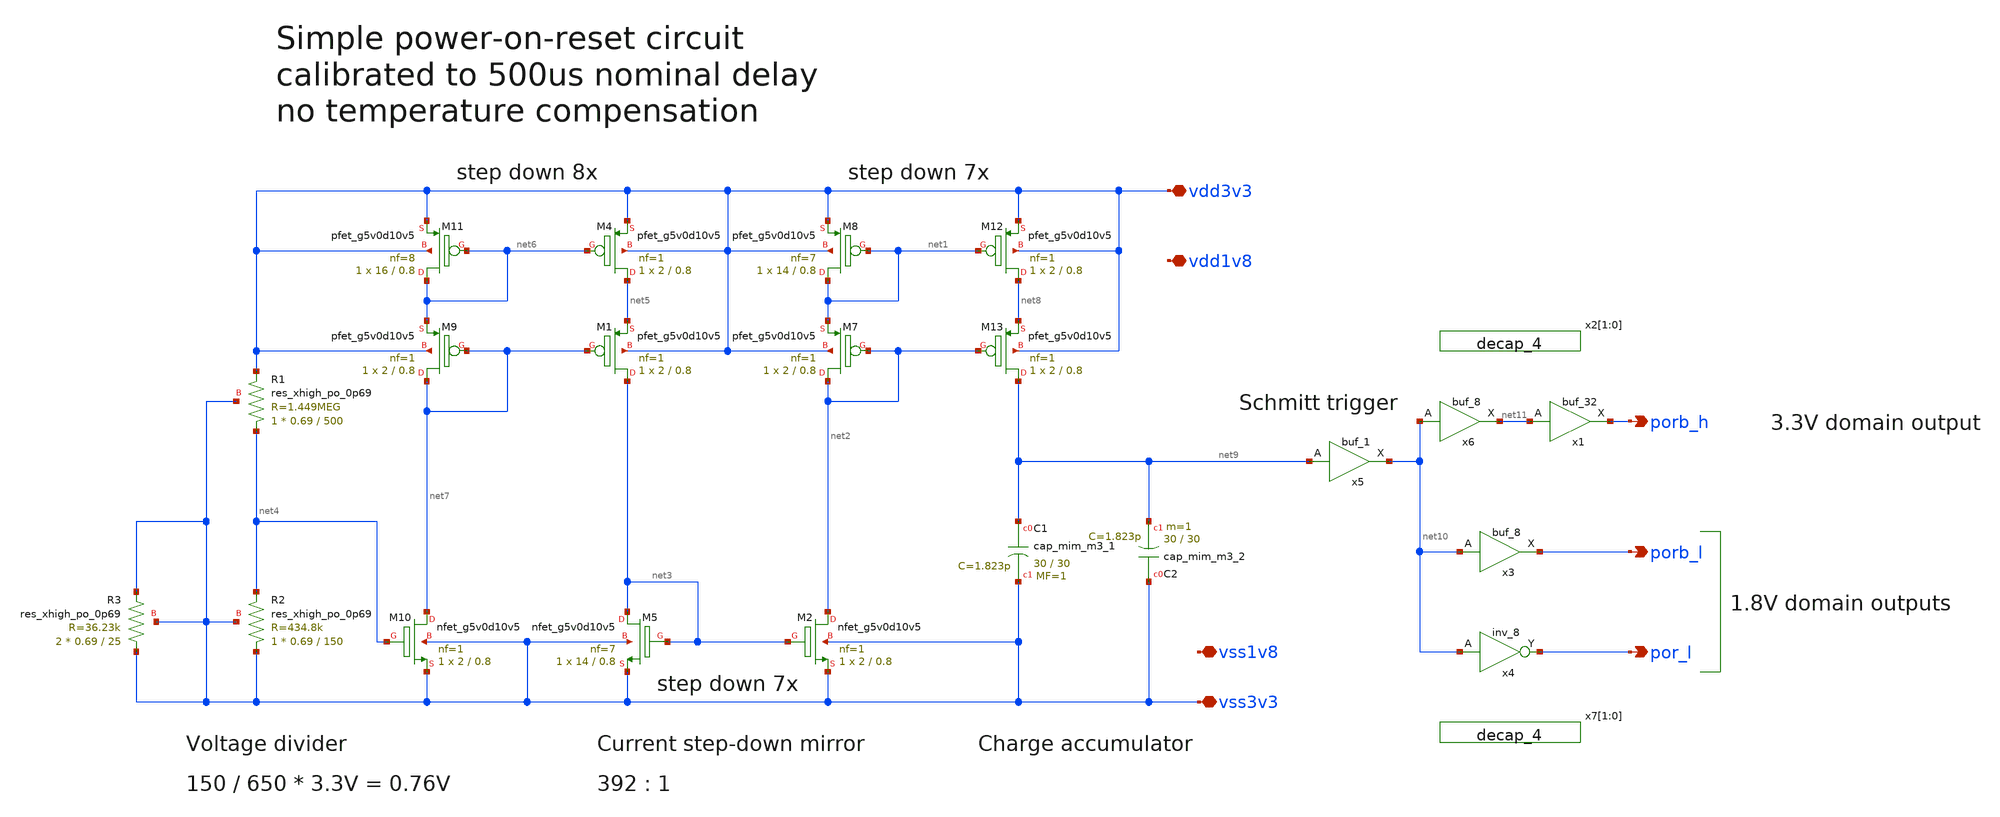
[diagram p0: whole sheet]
** sch_path: xschem/sky130_ef_ip__simple_por4x.sch
**.subckt sky130_ef_ip__simple_por4x vdd3v3 vss3v3 porb_l por_l vdd1v8 vss1v8 porb_h
*.iopin vdd3v3
*.iopin vss3v3
*.opin porb_l
*.opin por_l
*.iopin vdd1v8
*.iopin vss1v8
*.opin porb_h
XC1 net9 vss3v3 sky130_fd_pr__cap_mim_m3_1 W=30 L=30 MF=1 m=1
XC2 vss3v3 net9 sky130_fd_pr__cap_mim_m3_2 W=30 L=30 MF=1 m=1
XM1 net3 net7 net5 vdd3v3 sky130_fd_pr__pfet_g5v0d10v5 L=0.8 W=2 nf=1 ad='int((nf+1)/2) * W/nf * 0.29'
+ as='int((nf+2)/2) * W/nf * 0.29' pd='2*int((nf+1)/2) * (W/nf + 0.29)' ps='2*int((nf+2)/2) * (W/nf + 0.29)'
+ nrd='0.29 / W' nrs='0.29 / W' sa=0 sb=0 sd=0 mult=1 m=1
XM2 net2 net3 vss3v3 vss3v3 sky130_fd_pr__nfet_g5v0d10v5 L=0.8 W=2 nf=1 ad='int((nf+1)/2) * W/nf * 0.29'
+ as='int((nf+2)/2) * W/nf * 0.29' pd='2*int((nf+1)/2) * (W/nf + 0.29)' ps='2*int((nf+2)/2) * (W/nf + 0.29)'
+ nrd='0.29 / W' nrs='0.29 / W' sa=0 sb=0 sd=0 mult=1 m=1
XR1 net4 vdd3v3 vss3v3 sky130_fd_pr__res_xhigh_po_0p69 L=500 mult=1 m=1
XM4 net5 net6 vdd3v3 vdd3v3 sky130_fd_pr__pfet_g5v0d10v5 L=0.8 W=2 nf=1 ad='int((nf+1)/2) * W/nf * 0.29'
+ as='int((nf+2)/2) * W/nf * 0.29' pd='2*int((nf+1)/2) * (W/nf + 0.29)' ps='2*int((nf+2)/2) * (W/nf + 0.29)'
+ nrd='0.29 / W' nrs='0.29 / W' sa=0 sb=0 sd=0 mult=1 m=1
XM5 net3 net3 vss3v3 vss3v3 sky130_fd_pr__nfet_g5v0d10v5 L=0.8 W=14 nf=7 ad='int((nf+1)/2) * W/nf * 0.29'
+ as='int((nf+2)/2) * W/nf * 0.29' pd='2*int((nf+1)/2) * (W/nf + 0.29)' ps='2*int((nf+2)/2) * (W/nf + 0.29)'
+ nrd='0.29 / W' nrs='0.29 / W' sa=0 sb=0 sd=0 mult=1 m=1
XR2 vss3v3 net4 vss3v3 sky130_fd_pr__res_xhigh_po_0p69 L=150 mult=1 m=1
XM7 net2 net2 net1 vdd3v3 sky130_fd_pr__pfet_g5v0d10v5 L=0.8 W=2 nf=1 ad='int((nf+1)/2) * W/nf * 0.29'
+ as='int((nf+2)/2) * W/nf * 0.29' pd='2*int((nf+1)/2) * (W/nf + 0.29)' ps='2*int((nf+2)/2) * (W/nf + 0.29)'
+ nrd='0.29 / W' nrs='0.29 / W' sa=0 sb=0 sd=0 mult=1 m=1
XM8 net1 net1 vdd3v3 vdd3v3 sky130_fd_pr__pfet_g5v0d10v5 L=0.8 W=14 nf=7 ad='int((nf+1)/2) * W/nf * 0.29'
+ as='int((nf+2)/2) * W/nf * 0.29' pd='2*int((nf+1)/2) * (W/nf + 0.29)' ps='2*int((nf+2)/2) * (W/nf + 0.29)'
+ nrd='0.29 / W' nrs='0.29 / W' sa=0 sb=0 sd=0 mult=1 m=1
XM10 net7 net4 vss3v3 vss3v3 sky130_fd_pr__nfet_g5v0d10v5 L=0.8 W=2 nf=1 ad='int((nf+1)/2) * W/nf * 0.29'
+ as='int((nf+2)/2) * W/nf * 0.29' pd='2*int((nf+1)/2) * (W/nf + 0.29)' ps='2*int((nf+2)/2) * (W/nf + 0.29)'
+ nrd='0.29 / W' nrs='0.29 / W' sa=0 sb=0 sd=0 mult=1 m=1
XM9 net7 net7 net6 vdd3v3 sky130_fd_pr__pfet_g5v0d10v5 L=0.8 W=2 nf=1 ad='int((nf+1)/2) * W/nf * 0.29'
+ as='int((nf+2)/2) * W/nf * 0.29' pd='2*int((nf+1)/2) * (W/nf + 0.29)' ps='2*int((nf+2)/2) * (W/nf + 0.29)'
+ nrd='0.29 / W' nrs='0.29 / W' sa=0 sb=0 sd=0 mult=1 m=1
XM11 net6 net6 vdd3v3 vdd3v3 sky130_fd_pr__pfet_g5v0d10v5 L=0.8 W=16 nf=8 ad='int((nf+1)/2) * W/nf * 0.29'
+ as='int((nf+2)/2) * W/nf * 0.29' pd='2*int((nf+1)/2) * (W/nf + 0.29)' ps='2*int((nf+2)/2) * (W/nf + 0.29)'
+ nrd='0.29 / W' nrs='0.29 / W' sa=0 sb=0 sd=0 mult=1 m=1
XM12 net8 net1 vdd3v3 vdd3v3 sky130_fd_pr__pfet_g5v0d10v5 L=0.8 W=2 nf=1 ad='int((nf+1)/2) * W/nf * 0.29'
+ as='int((nf+2)/2) * W/nf * 0.29' pd='2*int((nf+1)/2) * (W/nf + 0.29)' ps='2*int((nf+2)/2) * (W/nf + 0.29)'
+ nrd='0.29 / W' nrs='0.29 / W' sa=0 sb=0 sd=0 mult=1 m=1
XM13 net9 net2 net8 vdd3v3 sky130_fd_pr__pfet_g5v0d10v5 L=0.8 W=2 nf=1 ad='int((nf+1)/2) * W/nf * 0.29'
+ as='int((nf+2)/2) * W/nf * 0.29' pd='2*int((nf+1)/2) * (W/nf + 0.29)' ps='2*int((nf+2)/2) * (W/nf + 0.29)'
+ nrd='0.29 / W' nrs='0.29 / W' sa=0 sb=0 sd=0 mult=1 m=1
XR3 vss3v3 vss3v3 vss3v3 sky130_fd_pr__res_xhigh_po_0p69 L=25 mult=2 m=2
x3 net10 vss1v8 vss1v8 vdd1v8 vdd1v8 porb_l sky130_fd_sc_hvl__buf_8
x4 net10 vss1v8 vss1v8 vdd1v8 vdd1v8 por_l sky130_fd_sc_hvl__inv_8
x5 net9 vss3v3 vss3v3 vdd3v3 vdd3v3 net10 sky130_fd_sc_hvl__schmittbuf_1
x6 net10 vss3v3 vss3v3 vdd3v3 vdd3v3 net11 sky130_fd_sc_hvl__buf_8
x1 net11 vss3v3 vss3v3 vdd3v3 vdd3v3 porb_h sky130_fd_sc_hvl__buf_32
x7[1] vss1v8 vss1v8 vdd1v8 vdd1v8 sky130_fd_sc_hvl__decap_4
x7[0] vss1v8 vss1v8 vdd1v8 vdd1v8 sky130_fd_sc_hvl__decap_4
x2[1] vss3v3 vss3v3 vdd3v3 vdd3v3 sky130_fd_sc_hvl__decap_4
x2[0] vss3v3 vss3v3 vdd3v3 vdd3v3 sky130_fd_sc_hvl__decap_4
**.ends
.end
